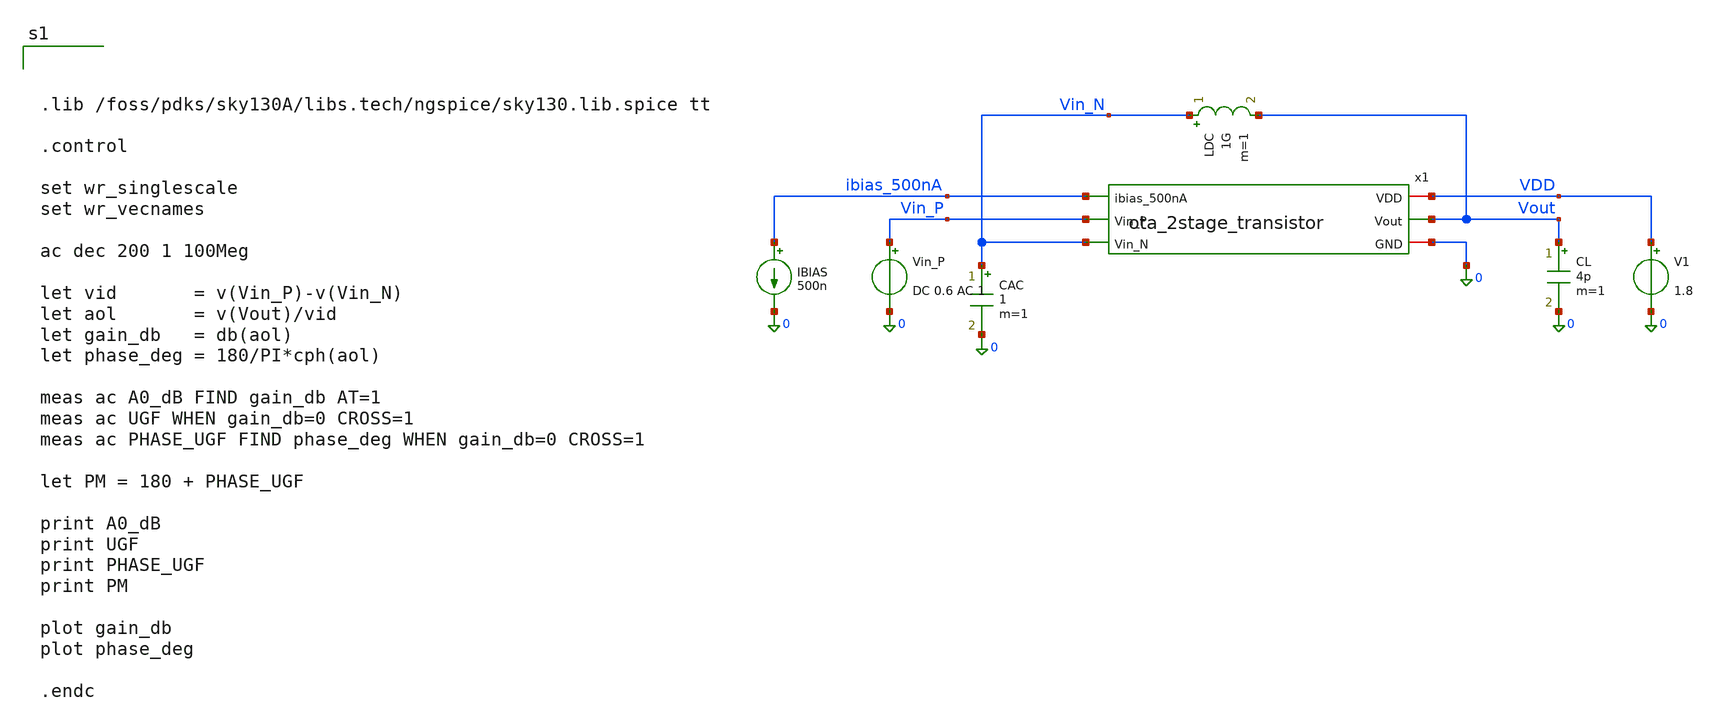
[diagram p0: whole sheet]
** sch_path: dfii/project_2stage_OTA_sim/tb_ota_2stage_ac.sch
**.subckt tb_ota_2stage_ac
x1 VDD ibias_500nA Vout Vin_P Vin_N 0 ota_2stage_transistor
V1 VDD 0 1.8
IBIAS ibias_500nA 0 500n
Vin_P Vin_P 0 DC 0.6 AC 1
CL Vout 0 4p m=1
LDC Vin_N Vout 1G m=1
CAC Vin_N 0 1 m=1
**** begin user architecture code



.lib /foss/pdks/sky130A/libs.tech/ngspice/sky130.lib.spice tt

.control

set wr_singlescale
set wr_vecnames

ac dec 200 1 100Meg

let vid       = v(Vin_P)-v(Vin_N)
let aol       = v(Vout)/vid
let gain_db   = db(aol)
let phase_deg = 180/PI*cph(aol)

meas ac A0_dB FIND gain_db AT=1
meas ac UGF WHEN gain_db=0 CROSS=1
meas ac PHASE_UGF FIND phase_deg WHEN gain_db=0 CROSS=1

let PM = 180 + PHASE_UGF

print A0_dB
print UGF
print PHASE_UGF
print PM

plot gain_db
plot phase_deg

.endc


**** end user architecture code
**.ends

* expanding   symbol:
*+  /foss/designs/project_2stage_OTA/dfii/project_2stage_OTA/ota_2stage_transistor.sym # of pins=6
** sym_path: dfii/project_2stage_OTA/ota_2stage_transistor.sym
** sch_path: dfii/project_2stage_OTA/ota_2stage_transistor.sch
.subckt ota_2stage_transistor VDD ibias_500nA Vout Vin_P Vin_N GND
*.iopin VDD
*.iopin GND
*.ipin ibias_500nA
*.ipin Vin_N
*.ipin Vin_P
*.opin Vout
XNLOAD_0 vdiode_n vdiode_n GND GND sky130_fd_pr__nfet_01v8 L=12 W=3.6 nf=1 ad='int((1 + 1)/2) * 3.6 / 1 * 0.29'
+ as='int((1 + 2)/2) * 3.6 / 1 * 0.29' pd='2*int((1 + 1)/2) * (3.6 / 1 + 0.29)' ps='2*int((1 + 2)/2) * (3.6 / 1 + 0.29)'
+ nrd='0.29 / 3.6 ' nrs='0.29 / 3.6 ' sa=0 sb=0 sd=0 mult=1 m=1
XNLOAD_1 out_s1 vdiode_n GND GND sky130_fd_pr__nfet_01v8 L=12 W=3.6 nf=1 ad='int((1 + 1)/2) * 3.6 / 1 * 0.29'
+ as='int((1 + 2)/2) * 3.6 / 1 * 0.29' pd='2*int((1 + 1)/2) * (3.6 / 1 + 0.29)' ps='2*int((1 + 2)/2) * (3.6 / 1 + 0.29)'
+ nrd='0.29 / 3.6 ' nrs='0.29 / 3.6 ' sa=0 sb=0 sd=0 mult=1 m=1
XNLOAD_2 Vout out_s1 GND GND sky130_fd_pr__nfet_01v8 L=2 W=3.6 nf=1 ad='int((1 + 1)/2) * 3.6 / 1 * 0.29'
+ as='int((1 + 2)/2) * 3.6 / 1 * 0.29' pd='2*int((1 + 1)/2) * (3.6 / 1 + 0.29)' ps='2*int((1 + 2)/2) * (3.6 / 1 + 0.29)'
+ nrd='0.29 / 3.6 ' nrs='0.29 / 3.6 ' sa=0 sb=0 sd=0 mult=2 m=2
XPDIFF_N vdiode_n Vin_N VCM VCM sky130_fd_pr__pfet_01v8 L=1 W=7.4 nf=1 ad='int((1 + 1)/2) * 7.4 / 1 * 0.29'
+ as='int((1 + 2)/2) * 7.4 / 1 * 0.29' pd='2*int((1 + 1)/2) * (7.4 / 1 + 0.29)' ps='2*int((1 + 2)/2) * (7.4 / 1 + 0.29)'
+ nrd='0.29 / 7.4 ' nrs='0.29 / 7.4 ' sa=0 sb=0 sd=0 mult=12 m=12
XPDIFF_P out_s1 Vin_P VCM VCM sky130_fd_pr__pfet_01v8 L=1 W=7.4 nf=1 ad='int((1 + 1)/2) * 7.4 / 1 * 0.29'
+ as='int((1 + 2)/2) * 7.4 / 1 * 0.29' pd='2*int((1 + 1)/2) * (7.4 / 1 + 0.29)' ps='2*int((1 + 2)/2) * (7.4 / 1 + 0.29)'
+ nrd='0.29 / 7.4 ' nrs='0.29 / 7.4 ' sa=0 sb=0 sd=0 mult=12 m=12
XPTAIL_1 VCM ibias_500nA VDD VDD sky130_fd_pr__pfet_01v8 L=1 W=1.76 nf=1 ad='int((1 + 1)/2) * 1.76 / 1 * 0.29'
+ as='int((1 + 2)/2) * 1.76 / 1 * 0.29' pd='2*int((1 + 1)/2) * (1.76 / 1 + 0.29)' ps='2*int((1 + 2)/2) * (1.76 / 1 + 0.29)'
+ nrd='0.29 / 1.76 ' nrs='0.29 / 1.76 ' sa=0 sb=0 sd=0 mult=1 m=1
XPTAIL_2 Vout ibias_500nA VDD VDD sky130_fd_pr__pfet_01v8 L=1 W=1.76 nf=1 ad='int((1 + 1)/2) * 1.76 / 1 * 0.29'
+ as='int((1 + 2)/2) * 1.76 / 1 * 0.29' pd='2*int((1 + 1)/2) * (1.76 / 1 + 0.29)' ps='2*int((1 + 2)/2) * (1.76 / 1 + 0.29)'
+ nrd='0.29 / 1.76 ' nrs='0.29 / 1.76 ' sa=0 sb=0 sd=0 mult=6 m=6
XPTAIL_0 ibias_500nA ibias_500nA VDD VDD sky130_fd_pr__pfet_01v8 L=1 W=1.76 nf=1 ad='int((1 + 1)/2) * 1.76 / 1 * 0.29'
+ as='int((1 + 2)/2) * 1.76 / 1 * 0.29' pd='2*int((1 + 1)/2) * (1.76 / 1 + 0.29)' ps='2*int((1 + 2)/2) * (1.76 / 1 + 0.29)'
+ nrd='0.29 / 1.76 ' nrs='0.29 / 1.76 ' sa=0 sb=0 sd=0 mult=1 m=1
XCMILLER out_s1 net1 sky130_fd_pr__cap_mim_m3_1 W=19 L=19 MF=1 m=1
XRMILLER Vout net1 GND sky130_fd_pr__res_xhigh_po_0p35 L=31.5 mult=1 m=1
.ends

.GLOBAL VDD
.end
